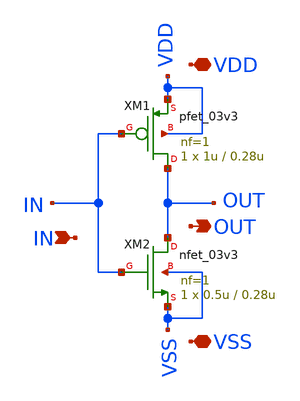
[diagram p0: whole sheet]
** sch_path: SCOP_INPUT_AND_MUX_PAKISTAN_03/Xschem/MUX_8x1/Inverter.sch
**.subckt Inverter IN OUT VDD VSS
*.ipin IN
*.opin OUT
*.iopin VDD
*.iopin VSS
XM1 OUT IN VDD VDD pfet_03v3 L=0.28u W=1u nf=1 ad='int((nf+1)/2) * W/nf * 0.18u' as='int((nf+2)/2) * W/nf * 0.18u'
+ pd='2*int((nf+1)/2) * (W/nf + 0.18u)' ps='2*int((nf+2)/2) * (W/nf + 0.18u)' nrd='0.18u / W' nrs='0.18u / W'
+ sa=0 sb=0 sd=0 m=1
XM2 OUT IN VSS VSS nfet_03v3 L=0.28u W=0.5u nf=1 ad='int((nf+1)/2) * W/nf * 0.18u' as='int((nf+2)/2) * W/nf * 0.18u'
+ pd='2*int((nf+1)/2) * (W/nf + 0.18u)' ps='2*int((nf+2)/2) * (W/nf + 0.18u)' nrd='0.18u / W' nrs='0.18u / W'
+ sa=0 sb=0 sd=0 m=1
**.ends
.end
